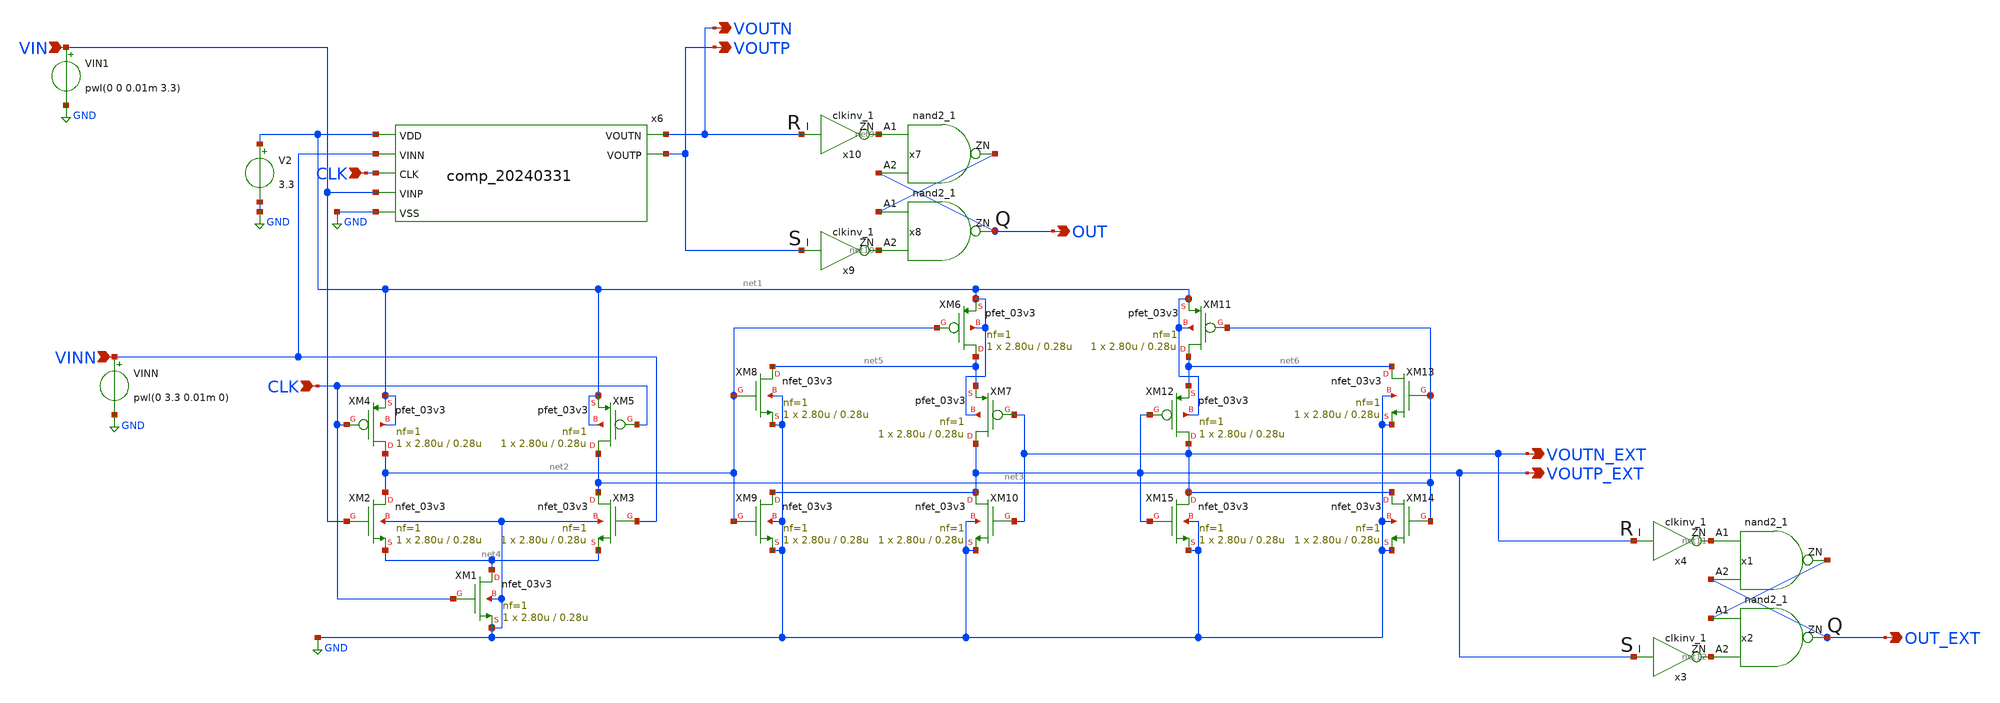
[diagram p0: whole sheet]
** sch_path: gitefu/tb/tb_like_p81.sch
**.subckt tb_like_p81 VIN VINN CLK CLK VOUTP_EXT VOUTN_EXT VOUTN VOUTP OUT OUT_EXT
*.ipin VIN
*.ipin VINN
*.ipin CLK
*.ipin CLK
*.opin VOUTP_EXT
*.opin VOUTN_EXT
*.opin VOUTN
*.opin VOUTP
*.opin OUT
*.opin OUT_EXT
VINN VINN GND pwl(0 3.3 0.01m 0)
V2 net1 GND 3.3
XM1 net4 CLK GND GND nfet_03v3 L=0.28u W=2.80u nf=1 ad='int((nf+1)/2) * W/nf * 0.18u' as='int((nf+2)/2) * W/nf * 0.18u'
+ pd='2*int((nf+1)/2) * (W/nf + 0.18u)' ps='2*int((nf+2)/2) * (W/nf + 0.18u)' nrd='0.18u / W' nrs='0.18u / W'
+ sa=0 sb=0 sd=0 m=1
XM2 net2 VIN net4 GND nfet_03v3 L=0.28u W=2.80u nf=1 ad='int((nf+1)/2) * W/nf * 0.18u' as='int((nf+2)/2) * W/nf * 0.18u'
+ pd='2*int((nf+1)/2) * (W/nf + 0.18u)' ps='2*int((nf+2)/2) * (W/nf + 0.18u)' nrd='0.18u / W' nrs='0.18u / W'
+ sa=0 sb=0 sd=0 m=1
XM4 net2 CLK net1 net1 pfet_03v3 L=0.28u W=2.80u nf=1 ad='int((nf+1)/2) * W/nf * 0.18u' as='int((nf+2)/2) * W/nf * 0.18u'
+ pd='2*int((nf+1)/2) * (W/nf + 0.18u)' ps='2*int((nf+2)/2) * (W/nf + 0.18u)' nrd='0.18u / W' nrs='0.18u / W'
+ sa=0 sb=0 sd=0 m=1
XM6 net5 net2 net1 net1 pfet_03v3 L=0.28u W=2.80u nf=1 ad='int((nf+1)/2) * W/nf * 0.18u' as='int((nf+2)/2) * W/nf * 0.18u'
+ pd='2*int((nf+1)/2) * (W/nf + 0.18u)' ps='2*int((nf+2)/2) * (W/nf + 0.18u)' nrd='0.18u / W' nrs='0.18u / W'
+ sa=0 sb=0 sd=0 m=1
XM7 VOUTP_EXT VOUTN_EXT net5 net1 pfet_03v3 L=0.28u W=2.80u nf=1 ad='int((nf+1)/2) * W/nf * 0.18u' as='int((nf+2)/2) * W/nf * 0.18u'
+ pd='2*int((nf+1)/2) * (W/nf + 0.18u)' ps='2*int((nf+2)/2) * (W/nf + 0.18u)' nrd='0.18u / W' nrs='0.18u / W'
+ sa=0 sb=0 sd=0 m=1
XM8 net5 net2 GND GND nfet_03v3 L=0.28u W=2.80u nf=1 ad='int((nf+1)/2) * W/nf * 0.18u' as='int((nf+2)/2) * W/nf * 0.18u'
+ pd='2*int((nf+1)/2) * (W/nf + 0.18u)' ps='2*int((nf+2)/2) * (W/nf + 0.18u)' nrd='0.18u / W' nrs='0.18u / W'
+ sa=0 sb=0 sd=0 m=1
XM9 VOUTP_EXT net2 GND GND nfet_03v3 L=0.28u W=2.80u nf=1 ad='int((nf+1)/2) * W/nf * 0.18u' as='int((nf+2)/2) * W/nf * 0.18u'
+ pd='2*int((nf+1)/2) * (W/nf + 0.18u)' ps='2*int((nf+2)/2) * (W/nf + 0.18u)' nrd='0.18u / W' nrs='0.18u / W'
+ sa=0 sb=0 sd=0 m=1
XM10 VOUTP_EXT VOUTN_EXT GND GND nfet_03v3 L=0.28u W=2.80u nf=1 ad='int((nf+1)/2) * W/nf * 0.18u' as='int((nf+2)/2) * W/nf * 0.18u'
+ pd='2*int((nf+1)/2) * (W/nf + 0.18u)' ps='2*int((nf+2)/2) * (W/nf + 0.18u)' nrd='0.18u / W' nrs='0.18u / W'
+ sa=0 sb=0 sd=0 m=1
XM3 net3 VINN net4 GND nfet_03v3 L=0.28u W=2.80u nf=1 ad='int((nf+1)/2) * W/nf * 0.18u' as='int((nf+2)/2) * W/nf * 0.18u'
+ pd='2*int((nf+1)/2) * (W/nf + 0.18u)' ps='2*int((nf+2)/2) * (W/nf + 0.18u)' nrd='0.18u / W' nrs='0.18u / W'
+ sa=0 sb=0 sd=0 m=1
XM5 net3 CLK net1 net1 pfet_03v3 L=0.28u W=2.80u nf=1 ad='int((nf+1)/2) * W/nf * 0.18u' as='int((nf+2)/2) * W/nf * 0.18u'
+ pd='2*int((nf+1)/2) * (W/nf + 0.18u)' ps='2*int((nf+2)/2) * (W/nf + 0.18u)' nrd='0.18u / W' nrs='0.18u / W'
+ sa=0 sb=0 sd=0 m=1
XM11 net6 net3 net1 net1 pfet_03v3 L=0.28u W=2.80u nf=1 ad='int((nf+1)/2) * W/nf * 0.18u' as='int((nf+2)/2) * W/nf * 0.18u'
+ pd='2*int((nf+1)/2) * (W/nf + 0.18u)' ps='2*int((nf+2)/2) * (W/nf + 0.18u)' nrd='0.18u / W' nrs='0.18u / W'
+ sa=0 sb=0 sd=0 m=1
XM12 VOUTN_EXT VOUTP_EXT net6 net1 pfet_03v3 L=0.28u W=2.80u nf=1 ad='int((nf+1)/2) * W/nf * 0.18u' as='int((nf+2)/2) * W/nf * 0.18u'
+ pd='2*int((nf+1)/2) * (W/nf + 0.18u)' ps='2*int((nf+2)/2) * (W/nf + 0.18u)' nrd='0.18u / W' nrs='0.18u / W'
+ sa=0 sb=0 sd=0 m=1
XM13 net6 net3 GND GND nfet_03v3 L=0.28u W=2.80u nf=1 ad='int((nf+1)/2) * W/nf * 0.18u' as='int((nf+2)/2) * W/nf * 0.18u'
+ pd='2*int((nf+1)/2) * (W/nf + 0.18u)' ps='2*int((nf+2)/2) * (W/nf + 0.18u)' nrd='0.18u / W' nrs='0.18u / W'
+ sa=0 sb=0 sd=0 m=1
XM14 VOUTN_EXT net3 GND GND nfet_03v3 L=0.28u W=2.80u nf=1 ad='int((nf+1)/2) * W/nf * 0.18u' as='int((nf+2)/2) * W/nf * 0.18u'
+ pd='2*int((nf+1)/2) * (W/nf + 0.18u)' ps='2*int((nf+2)/2) * (W/nf + 0.18u)' nrd='0.18u / W' nrs='0.18u / W'
+ sa=0 sb=0 sd=0 m=1
XM15 VOUTN_EXT VOUTP_EXT GND GND nfet_03v3 L=0.28u W=2.80u nf=1 ad='int((nf+1)/2) * W/nf * 0.18u' as='int((nf+2)/2) * W/nf * 0.18u'
+ pd='2*int((nf+1)/2) * (W/nf + 0.18u)' ps='2*int((nf+2)/2) * (W/nf + 0.18u)' nrd='0.18u / W' nrs='0.18u / W'
+ sa=0 sb=0 sd=0 m=1
x6 net1 CLK VOUTP VOUTN VIN VINN GND TOP
x7 net9 OUT net7 VDD VDD 0 0 gf180mcu_fd_sc_mcu7t5v0__nand2_1
x8 net7 net10 OUT VDD VDD 0 0 gf180mcu_fd_sc_mcu7t5v0__nand2_1
x9 VOUTP net10 VDD VDD 0 0 gf180mcu_fd_sc_mcu7t5v0__clkinv_1
x10 VOUTN net9 VDD VDD 0 0 gf180mcu_fd_sc_mcu7t5v0__clkinv_1
VIN1 VIN GND pwl(0 0 0.01m 3.3)
x1 net11 OUT_EXT net8 VDD VDD 0 0 gf180mcu_fd_sc_mcu7t5v0__nand2_1
x2 net8 net12 OUT_EXT VDD VDD 0 0 gf180mcu_fd_sc_mcu7t5v0__nand2_1
x3 VOUTP_EXT net12 VDD VDD 0 0 gf180mcu_fd_sc_mcu7t5v0__clkinv_1
x4 VOUTN_EXT net11 VDD VDD 0 0 gf180mcu_fd_sc_mcu7t5v0__clkinv_1
**** begin user architecture code



VDD CLK 0 pulse (0 3.3 0 40p 40p 62.5n 125n) dc 0v
.include /media/tomoakitanaka/Documents/MyDocuments/personal/ISHIKAI/2024/Chipathon2023_ADC/gitefu/comp_20240331/TOP_pex_extracted.spice
.control
set wr_vecnames
set wr_singlescale
let count=0
dowhile count < 10
  save VIN VINN OUT_EXT OUT
  tran 10n 0.01m
  write VOUT_EXT.raw
  set appendwrite
  reset
  let count = count + 1
end
.endc




.include $::180MCU_MODELS/design.ngspice
.lib $::180MCU_MODELS/sm141064.ngspice typical
.include $::180MCU_STDCELLS/gf180mcu_fd_sc_mcu7t5v0.spice
.param   sw_stat_global = 0   sw_stat_mismatch = 1
**
********* Default mc skew value *********
**  mc_skew = 3  res_mc_skew = 3  cap_mc_skew = 3
**
****** Default flicker noise corner switch *****
**   fnoicor = 0

**** end user architecture code
**.ends
.GLOBAL GND
.end
